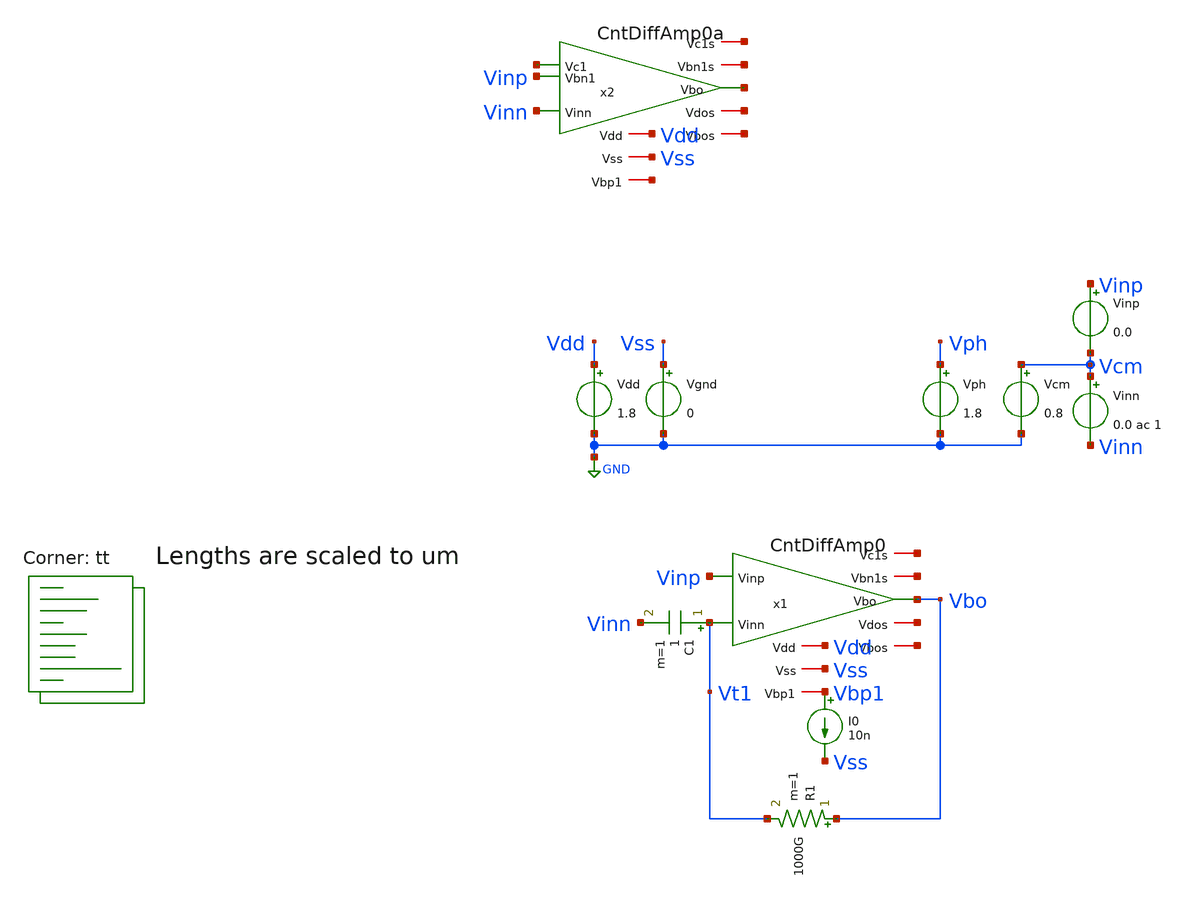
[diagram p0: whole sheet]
** sch_path: ic/CntDiffAmp/Testbench/CntDiffAmp0_tb.sch
**.subckt CntDiffAmp0_tb
I0 Vbp1 Vss 10n
Vdd Vdd GND 1.8
Vgnd Vss GND 0
Vinp Vinp Vcm 0.0
Vinn Vcm Vinn 0.0 ac 1
Vph Vph GND 1.8
Vcm Vcm GND 0.8
x1 Vdd Vss Vbo Vinp Vt1 Vbp1 net1 net2 net3 net4 CntDiffAmp0
R1 Vbo Vt1 1000G m=1
C1 Vt1 Vinn 1 m=1
x2 Vdd Vss net5 net6 Vinn net7 net8 net9 net10 net11 Vinp CntDiffAmp0a
**** begin user architecture code
.lib $::SKYWATER_MODELS/sky130.lib.spice tt

* this option enables mos model bin
* selection based on W/NF instead of W
.option wnflag=1
.option savecurrents acct abstol=1e-15
*reltol=1e-6
*gmin=1e-15

.control
save all
save @m.x1.xm1.msky130_fd_pr__pfet_01v8_lvt[gm]
save @m.x1.xm1.msky130_fd_pr__pfet_01v8_lvt[vth]
save @m.x1.xm1.msky130_fd_pr__pfet_01v8_lvt[vdsat]
save @m.x1.xm2.msky130_fd_pr__pfet_01v8_lvt[gm]
save @m.x1.xm2.msky130_fd_pr__pfet_01v8_lvt[vth]
save @m.x1.xm2.msky130_fd_pr__pfet_01v8_lvt[vdsat]
save @m.x1.xm4.msky130_fd_pr__nfet_01v8_lvt[gm]
save @m.x1.xm4.msky130_fd_pr__nfet_01v8_lvt[vth]
save @m.x1.xm4.msky130_fd_pr__nfet_01v8_lvt[vdsat]

op
write CntDiffAmp0_tb.raw

dc Vcm 0.0 1.8 0.01
plot v(x1.Vbn1), v(x1.Vc1), v(x1.Vdo), v(Vbp1), v(Vbo) vs v(Vcm)
plot i(v.x1.Vm1) vs v(Vcm)
plot @m.x1.xm2.msky130_fd_pr__pfet_01v8_lvt[gm], @m.x1.xm4.msky130_fd_pr__nfet_01v8_lvt[gm] vs
+ V(Vcm)

set appendwrite
write CntDiffAmp0_tb.raw

ac dec 10 1 1e9
plot vdb(x1.Vdo), vdb(Vbo)

write CntDiffAmp0_tb.raw
.endc




** CntFET model
.subckt cntnfet_a d g s b
.param l=1 w=0.01 mult=1
mcntnfet_a d g s b cntnfet l={l} w={w}
* BSIM4 model
.model cntnfet nmos  level=54 version=4.8.2  toxe=7e-9
.ends cntnfet_a

.subckt cntpfet_a d g s b
.param l=1 w=0.01 mult=1
mcntpfet_a d g s b cntpfet l={l} w={w}
* BSIM4 model
.model cntpfet pmos  level=54 version=4.8.2  toxe=100e-9 U0=1.09e-4 VTH0=-2.02
.ends cntnfet_a

.model cntnfet_b nmos level=54 version=4.8.2 toxe=5e-9
.model cntpfet_b nmos level=54 version=4.8.2 toxe=5e-9


**** end user architecture code
**.ends

* expanding   symbol:  ../Schematic/CntDiffAmp0.sym # of pins=10
** sym_path: ic/CntDiffAmp/Schematic/CntDiffAmp0.sym
** sch_path: ic/CntDiffAmp/Schematic/CntDiffAmp0.sch
.subckt CntDiffAmp0 Vdd Vss Vbo Vinp Vinn Vbp1 Vc1s Vbn1s Vdos Vbos
*.ipin Vinp
*.opin Vbo
*.ipin Vinn
*.iopin Vdd
*.iopin Vss
*.iopin Vbp1
*.opin Vc1s
*.opin Vbn1s
*.opin Vdos
*.opin Vbos
XM5 Vdo Vbn1 Vss Vss sky130_fd_pr__nfet_01v8_lvt L=1 W=5 nf=1 ad='int((nf+1)/2) * W/nf * 0.29' as='int((nf+2)/2) * W/nf * 0.29'
+ pd='2*int((nf+1)/2) * (W/nf + 0.29)' ps='2*int((nf+2)/2) * (W/nf + 0.29)' nrd='0.29 / W' nrs='0.29 / W'
+ sa=0 sb=0 sd=0 mult=1 m=1
XM4 Vbn1 Vbn1 Vss Vss sky130_fd_pr__nfet_01v8_lvt L=1 W=5 nf=1 ad='int((nf+1)/2) * W/nf * 0.29' as='int((nf+2)/2) * W/nf * 0.29'
+ pd='2*int((nf+1)/2) * (W/nf + 0.29)' ps='2*int((nf+2)/2) * (W/nf + 0.29)' nrd='0.29 / W' nrs='0.29 / W'
+ sa=0 sb=0 sd=0 mult=1 m=1
XM1 Vc1 Vbp1 Vdd Vdd sky130_fd_pr__pfet_01v8_lvt L=2 W=1 nf=1 ad='int((nf+1)/2) * W/nf * 0.29' as='int((nf+2)/2) * W/nf * 0.29'
+ pd='2*int((nf+1)/2) * (W/nf + 0.29)' ps='2*int((nf+2)/2) * (W/nf + 0.29)' nrd='0.29 / W' nrs='0.29 / W'
+ sa=0 sb=0 sd=0 mult=1 m=1
XM6 Vbp1 Vbp1 Vdd Vdd sky130_fd_pr__pfet_01v8_lvt L=2 W=10 nf=1 ad='int((nf+1)/2) * W/nf * 0.29' as='int((nf+2)/2) * W/nf * 0.29'
+ pd='2*int((nf+1)/2) * (W/nf + 0.29)' ps='2*int((nf+2)/2) * (W/nf + 0.29)' nrd='0.29 / W' nrs='0.29 / W'
+ sa=0 sb=0 sd=0 mult=1 m=1
XM2 Vbn1 Vinp Vc1 Vdd sky130_fd_pr__pfet_01v8_lvt L=2 W=10 nf=1 ad='int((nf+1)/2) * W/nf * 0.29' as='int((nf+2)/2) * W/nf * 0.29'
+ pd='2*int((nf+1)/2) * (W/nf + 0.29)' ps='2*int((nf+2)/2) * (W/nf + 0.29)' nrd='0.29 / W' nrs='0.29 / W'
+ sa=0 sb=0 sd=0 mult=1 m=1
XM3 Vdo Vinn Vc1 Vdd sky130_fd_pr__pfet_01v8_lvt L=2 W=10 nf=1 ad='int((nf+1)/2) * W/nf * 0.29' as='int((nf+2)/2) * W/nf * 0.29'
+ pd='2*int((nf+1)/2) * (W/nf + 0.29)' ps='2*int((nf+2)/2) * (W/nf + 0.29)' nrd='0.29 / W' nrs='0.29 / W'
+ sa=0 sb=0 sd=0 mult=1 m=1
XM7 net2 Vbp1 Vdd Vdd sky130_fd_pr__pfet_01v8_lvt L=2 W=100 nf=10 ad='int((nf+1)/2) * W/nf * 0.29' as='int((nf+2)/2) * W/nf * 0.29'
+ pd='2*int((nf+1)/2) * (W/nf + 0.29)' ps='2*int((nf+2)/2) * (W/nf + 0.29)' nrd='0.29 / W' nrs='0.29 / W'
+ sa=0 sb=0 sd=0 mult=1 m=1
XM8 Vbo Vdo Vss Vss sky130_fd_pr__nfet_01v8_lvt L=1 W=100 nf=10 ad='int((nf+1)/2) * W/nf * 0.29' as='int((nf+2)/2) * W/nf * 0.29'
+ pd='2*int((nf+1)/2) * (W/nf + 0.29)' ps='2*int((nf+2)/2) * (W/nf + 0.29)' nrd='0.29 / W' nrs='0.29 / W'
+ sa=0 sb=0 sd=0 mult=1 m=1
Vm1 net2 Vbo 0
.save i(vm1)
XM9 Vdd Vc1 Vc1s Vss sky130_fd_pr__nfet_01v8_lvt L=1 W=10 nf=1 ad='int((nf+1)/2) * W/nf * 0.29' as='int((nf+2)/2) * W/nf * 0.29'
+ pd='2*int((nf+1)/2) * (W/nf + 0.29)' ps='2*int((nf+2)/2) * (W/nf + 0.29)' nrd='0.29 / W' nrs='0.29 / W'
+ sa=0 sb=0 sd=0 mult=1 m=1
XM10 Vss Vbn1 Vbn1s Vdd sky130_fd_pr__pfet_01v8_lvt L=2 W=10 nf=1 ad='int((nf+1)/2) * W/nf * 0.29' as='int((nf+2)/2) * W/nf * 0.29'
+ pd='2*int((nf+1)/2) * (W/nf + 0.29)' ps='2*int((nf+2)/2) * (W/nf + 0.29)' nrd='0.29 / W' nrs='0.29 / W'
+ sa=0 sb=0 sd=0 mult=1 m=1
XM11 Vdd Vbo Vbos Vss sky130_fd_pr__nfet_01v8_lvt L=1 W=100 nf=10 ad='int((nf+1)/2) * W/nf * 0.29' as='int((nf+2)/2) * W/nf * 0.29'
+ pd='2*int((nf+1)/2) * (W/nf + 0.29)' ps='2*int((nf+2)/2) * (W/nf + 0.29)' nrd='0.29 / W' nrs='0.29 / W'
+ sa=0 sb=0 sd=0 mult=1 m=1
XM12 Vss Vdo Vdos Vdd sky130_fd_pr__pfet_01v8_lvt L=2 W=10 nf=1 ad='int((nf+1)/2) * W/nf * 0.29' as='int((nf+2)/2) * W/nf * 0.29'
+ pd='2*int((nf+1)/2) * (W/nf + 0.29)' ps='2*int((nf+2)/2) * (W/nf + 0.29)' nrd='0.29 / W' nrs='0.29 / W'
+ sa=0 sb=0 sd=0 mult=1 m=1
.ends


* expanding   symbol:  ../Schematic/CntDiffAmp0a.sym # of pins=11
** sym_path: ic/CntDiffAmp/Schematic/CntDiffAmp0a.sym
** sch_path: ic/CntDiffAmp/Schematic/CntDiffAmp0a.sch
.subckt CntDiffAmp0a Vdd Vss Vbo Vc1 Vinn Vbp1 Vc1s Vbn1s Vdos Vbos Vbn1
*.iopin Vc1
*.opin Vbo
*.ipin Vinn
*.iopin Vdd
*.iopin Vss
*.iopin Vbp1
*.opin Vc1s
*.opin Vbn1s
*.opin Vdos
*.opin Vbos
*.iopin Vbn1
XM5 Vdo Vbn1 Vss Vss sky130_fd_pr__nfet_01v8_lvt L=1 W=5 nf=1 ad='int((nf+1)/2) * W/nf * 0.29' as='int((nf+2)/2) * W/nf * 0.29'
+ pd='2*int((nf+1)/2) * (W/nf + 0.29)' ps='2*int((nf+2)/2) * (W/nf + 0.29)' nrd='0.29 / W' nrs='0.29 / W'
+ sa=0 sb=0 sd=0 mult=1 m=1
XM4 Vbn1 Vbn1 Vss Vss sky130_fd_pr__nfet_01v8_lvt L=1 W=5 nf=1 ad='int((nf+1)/2) * W/nf * 0.29' as='int((nf+2)/2) * W/nf * 0.29'
+ pd='2*int((nf+1)/2) * (W/nf + 0.29)' ps='2*int((nf+2)/2) * (W/nf + 0.29)' nrd='0.29 / W' nrs='0.29 / W'
+ sa=0 sb=0 sd=0 mult=1 m=1
XM1 Vc1 Vbp1 Vdd Vdd sky130_fd_pr__pfet_01v8_lvt L=2 W=1 nf=1 ad='int((nf+1)/2) * W/nf * 0.29' as='int((nf+2)/2) * W/nf * 0.29'
+ pd='2*int((nf+1)/2) * (W/nf + 0.29)' ps='2*int((nf+2)/2) * (W/nf + 0.29)' nrd='0.29 / W' nrs='0.29 / W'
+ sa=0 sb=0 sd=0 mult=1 m=1
XM6 Vbp1 Vbp1 Vdd Vdd sky130_fd_pr__pfet_01v8_lvt L=2 W=10 nf=1 ad='int((nf+1)/2) * W/nf * 0.29' as='int((nf+2)/2) * W/nf * 0.29'
+ pd='2*int((nf+1)/2) * (W/nf + 0.29)' ps='2*int((nf+2)/2) * (W/nf + 0.29)' nrd='0.29 / W' nrs='0.29 / W'
+ sa=0 sb=0 sd=0 mult=1 m=1
XM3 Vdo Vinn Vc1 Vdd sky130_fd_pr__pfet_01v8_lvt L=2 W=10 nf=1 ad='int((nf+1)/2) * W/nf * 0.29' as='int((nf+2)/2) * W/nf * 0.29'
+ pd='2*int((nf+1)/2) * (W/nf + 0.29)' ps='2*int((nf+2)/2) * (W/nf + 0.29)' nrd='0.29 / W' nrs='0.29 / W'
+ sa=0 sb=0 sd=0 mult=1 m=1
XM7 net2 Vbp1 Vdd Vdd sky130_fd_pr__pfet_01v8_lvt L=2 W=100 nf=10 ad='int((nf+1)/2) * W/nf * 0.29' as='int((nf+2)/2) * W/nf * 0.29'
+ pd='2*int((nf+1)/2) * (W/nf + 0.29)' ps='2*int((nf+2)/2) * (W/nf + 0.29)' nrd='0.29 / W' nrs='0.29 / W'
+ sa=0 sb=0 sd=0 mult=1 m=1
XM8 Vbo Vdo Vss Vss sky130_fd_pr__nfet_01v8_lvt L=1 W=100 nf=10 ad='int((nf+1)/2) * W/nf * 0.29' as='int((nf+2)/2) * W/nf * 0.29'
+ pd='2*int((nf+1)/2) * (W/nf + 0.29)' ps='2*int((nf+2)/2) * (W/nf + 0.29)' nrd='0.29 / W' nrs='0.29 / W'
+ sa=0 sb=0 sd=0 mult=1 m=1
Vm1 net2 Vbo 0
.save i(vm1)
XM9 Vdd Vc1 Vc1s Vss sky130_fd_pr__nfet_01v8_lvt L=1 W=10 nf=1 ad='int((nf+1)/2) * W/nf * 0.29' as='int((nf+2)/2) * W/nf * 0.29'
+ pd='2*int((nf+1)/2) * (W/nf + 0.29)' ps='2*int((nf+2)/2) * (W/nf + 0.29)' nrd='0.29 / W' nrs='0.29 / W'
+ sa=0 sb=0 sd=0 mult=1 m=1
XM10 Vss Vbn1 Vbn1s Vdd sky130_fd_pr__pfet_01v8_lvt L=2 W=10 nf=1 ad='int((nf+1)/2) * W/nf * 0.29' as='int((nf+2)/2) * W/nf * 0.29'
+ pd='2*int((nf+1)/2) * (W/nf + 0.29)' ps='2*int((nf+2)/2) * (W/nf + 0.29)' nrd='0.29 / W' nrs='0.29 / W'
+ sa=0 sb=0 sd=0 mult=1 m=1
XM11 Vdd Vbo Vbos Vss sky130_fd_pr__nfet_01v8_lvt L=1 W=100 nf=10 ad='int((nf+1)/2) * W/nf * 0.29' as='int((nf+2)/2) * W/nf * 0.29'
+ pd='2*int((nf+1)/2) * (W/nf + 0.29)' ps='2*int((nf+2)/2) * (W/nf + 0.29)' nrd='0.29 / W' nrs='0.29 / W'
+ sa=0 sb=0 sd=0 mult=1 m=1
XM12 Vss Vdo Vdos Vdd sky130_fd_pr__pfet_01v8_lvt L=2 W=10 nf=1 ad='int((nf+1)/2) * W/nf * 0.29' as='int((nf+2)/2) * W/nf * 0.29'
+ pd='2*int((nf+1)/2) * (W/nf + 0.29)' ps='2*int((nf+2)/2) * (W/nf + 0.29)' nrd='0.29 / W' nrs='0.29 / W'
+ sa=0 sb=0 sd=0 mult=1 m=1
.ends

.GLOBAL GND
.end
